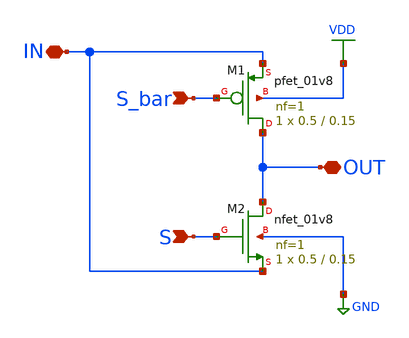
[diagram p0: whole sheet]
** sch_path: mux_xshcem/tg.sch
**.subckt tg OUT IN S S_bar
*.iopin OUT
*.iopin IN
*.ipin S
*.ipin S_bar
XM1 OUT S_bar IN VDD sky130_fd_pr__pfet_01v8 L=0.15 W=0.5 nf=1 ad='int((1 + 1)/2) * 0.5 / 1 * 0.29' as='int((1 + 2)/2) * 0.5 / 1 * 0.29'
+ pd='2*int((1 + 1)/2) * (0.5 / 1 + 0.29)' ps='2*int((1 + 2)/2) * (0.5 / 1 + 0.29)' nrd='0.29 / 0.5 ' nrs='0.29 / 0.5 '
+ sa=0 sb=0 sd=0 mult=1 m=1
XM2 OUT S IN GND sky130_fd_pr__nfet_01v8 L=0.15 W=0.5 nf=1 ad='int((1 + 1)/2) * 0.5 / 1 * 0.29' as='int((1 + 2)/2) * 0.5 / 1 * 0.29'
+ pd='2*int((1 + 1)/2) * (0.5 / 1 + 0.29)' ps='2*int((1 + 2)/2) * (0.5 / 1 + 0.29)' nrd='0.29 / 0.5 ' nrs='0.29 / 0.5 '
+ sa=0 sb=0 sd=0 mult=1 m=1
**.ends
.GLOBAL VDD
.GLOBAL GND
.end
